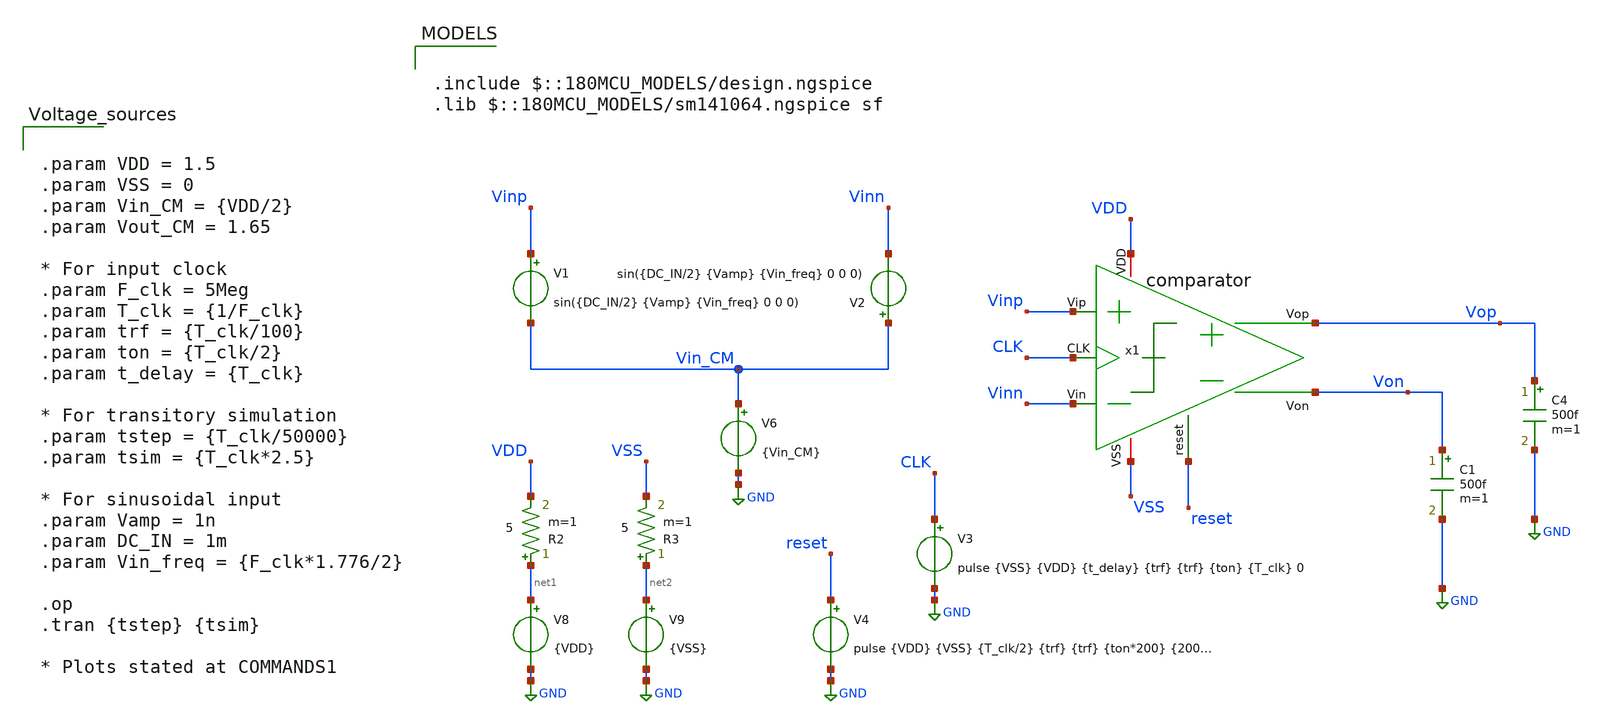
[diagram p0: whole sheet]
** sch_path: designs/DS_modulator/comparator/xschem/DSM_SA_Comparator_TB.sch
**.subckt DSM_SA_Comparator_TB
V6 Vin_CM GND {Vin_CM}
V8 net1 GND {VDD}
V9 net2 GND {VSS}
C4 Vop GND 500f m=1
C1 Von GND 500f m=1
V1 Vinp Vin_CM sin({DC_IN/2} {Vamp} {Vin_freq} 0 0 0)
V2 Vin_CM Vinn sin({DC_IN/2} {Vamp} {Vin_freq} 0 0 0)
V3 CLK GND pulse {VSS} {VDD} {t_delay} {trf} {trf} {ton} {T_clk} 0
V4 reset GND pulse {VDD} {VSS} {T_clk/2} {trf} {trf} {ton*200} {200*T_clk} 0
x1 VDD CLK Vop reset Von Vinp Vinn VSS comparator
R2 net1 VDD 5 m=1
R3 net2 VSS 5 m=1
**** begin user architecture code

.include $::180MCU_MODELS/design.ngspice
.lib $::180MCU_MODELS/sm141064.ngspice sf



.param VDD = 1.5
.param VSS = 0
.param Vin_CM = {VDD/2}
.param Vout_CM = 1.65

* For input clock
.param F_clk = 5Meg
.param T_clk = {1/F_clk}
.param trf = {T_clk/100}
.param ton = {T_clk/2}
.param t_delay = {T_clk}

* For transitory simulation
.param tstep = {T_clk/50000}
.param tsim = {T_clk*2.5}

* For sinusoidal input
.param Vamp = 1n
.param DC_IN = 1m
.param Vin_freq = {F_clk*1.776/2}

.op
.tran {tstep} {tsim}

* Plots stated at COMMANDS1





.control
savel all
run

plot x1.vx x1.vy x1.vp x1.vq
plot reset clk vinp vinn
plot x1.reset_bb x1.vx_b x1.reset_b+2 x1.vy_b+2 vop+4 von+4

.endc



**** end user architecture code
**.ends
.GLOBAL GND
.end
